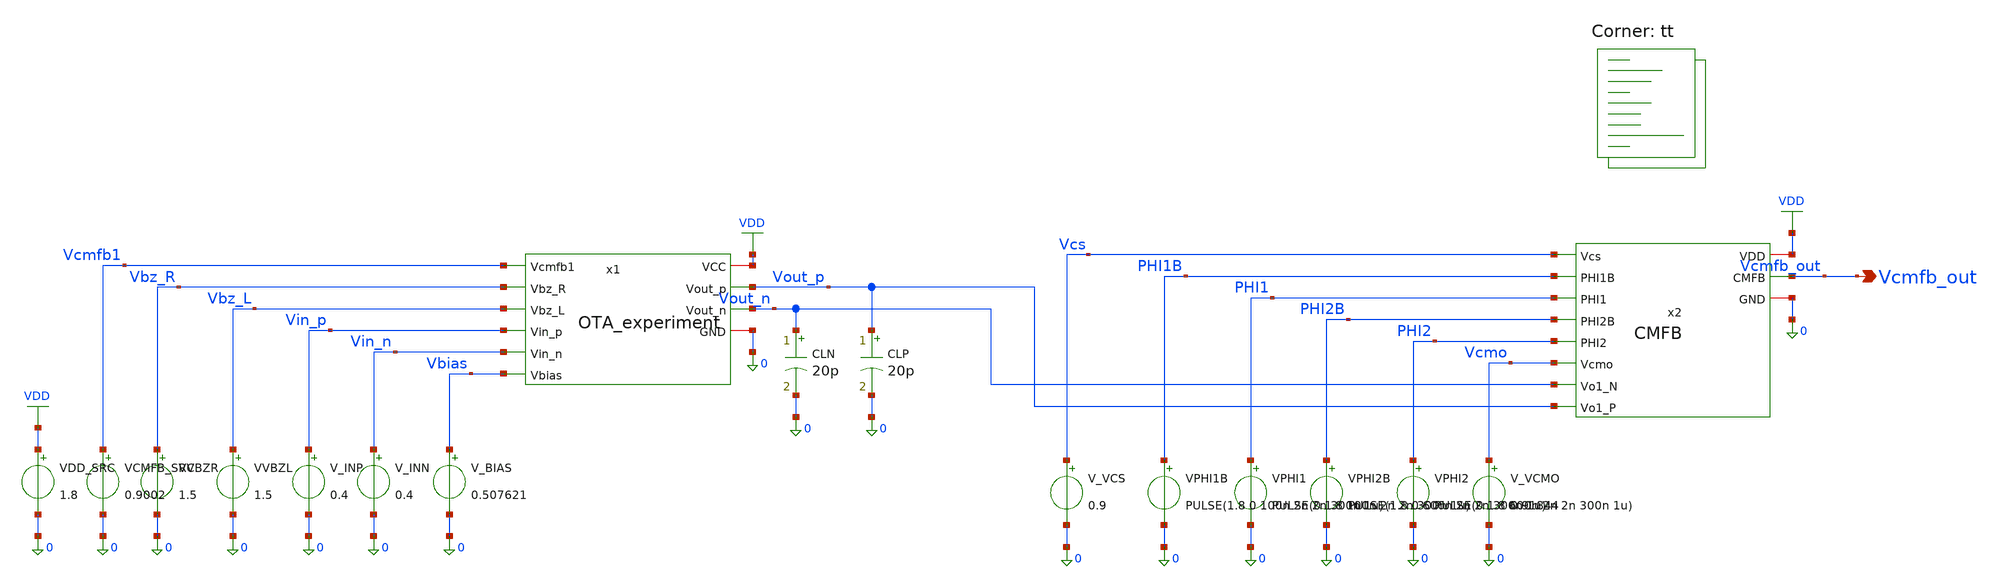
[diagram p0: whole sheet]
** sch_path: blocks/02_CMFB/sim/tb_OTA_CMFB_sign.sch
**.subckt tb_OTA_CMFB_sign Vcmfb_out
*.opin Vcmfb_out
VDD_SRC VDD 0 1.8
VCMFB_SRC Vcmfb1 0 0.9002
VVBZR Vbz_R 0 1.5
VVBZL Vbz_L 0 1.5
V_INP Vin_p 0 0.4
V_INN Vin_n 0 0.4
V_BIAS Vbias 0 0.507621
x1 VDD Vcmfb1 Vbz_R Vbz_L Vin_p Vin_n Vout_p Vout_n Vbias 0 OTA_experiment
CLP Vout_p 0 20p m=1
CLN Vout_n 0 20p m=1
V_VCS Vcs 0 0.9
VPHI1B PHI1B 0 PULSE(1.8 0 100n 2n 2n 300n 1u)
VPHI1 PHI1 0 PULSE(0 1.8 100n 2n 2n 300n 1u)
VPHI2B PHI2B 0 PULSE(1.8 0 600n 2n 2n 300n 1u)
VPHI2 PHI2 0 PULSE(0 1.8 600n 2n 2n 300n 1u)
V_VCMO Vcmo 0 0.91844
x2 Vcmfb_out Vcs PHI1B PHI1 VDD PHI2B 0 PHI2 Vcmo Vout_n Vout_p CMFB
**** begin user architecture code
.lib $::SKYWATER_MODELS/sky130.lib.spice tt


.options rshunt=1e12

RLEAK_OUT Vcmfb_out 0 1e12

.control
save all

* ==========================================================
* STEP 1: TRUE DC OPERATING POINT
* ==========================================================

op

let VOCM_OP = (v(vout_p)+v(vout_n))/2
let VOD_OP  = v(vout_p)-v(vout_n)

print v(vcmfb1)
print v(vout_p)
print v(vout_n)
print VOCM_OP
print VOD_OP


* ==========================================================
* STEP 2: TRANSIENT
*
* IMPORTANT:
* THERE IS NO UIC HERE.
* ==========================================================

tran 1n 10u

let VOCM = (v(vout_p)+v(vout_n))/2
let VOD  = v(vout_p)-v(vout_n)


* ==========================================================
* OTA STEADY-STATE CHARACTERIZATION
* ==========================================================

meas tran VOUTP_AVG AVG v(vout_p) FROM=8u TO=10u
meas tran VOUTN_AVG AVG v(vout_n) FROM=8u TO=10u

meas tran VOCM_AVG AVG VOCM FROM=8u TO=10u
meas tran VOCM_MIN MIN VOCM FROM=8u TO=10u
meas tran VOCM_MAX MAX VOCM FROM=8u TO=10u

meas tran VOD_AVG AVG VOD FROM=8u TO=10u


* ==========================================================
* EXTERNAL OTA CMFB CONTROL
* ==========================================================

meas tran VCMFB_IN_AVG AVG v(vcmfb1) FROM=8u TO=10u


* ==========================================================
* SC-CMFB OUTPUT CHARACTERIZATION
* ==========================================================

meas tran VCMFB_OUT_AVG AVG v(vcmfb_out) FROM=8u TO=10u
meas tran VCMFB_OUT_MIN MIN v(vcmfb_out) FROM=8u TO=10u
meas tran VCMFB_OUT_MAX MAX v(vcmfb_out) FROM=8u TO=10u

let VCMFB_OUT_RIPPLE = VCMFB_OUT_MAX-VCMFB_OUT_MIN

let VCMFB_OUT_ERROR = VCMFB_OUT_AVG-0.9


* ==========================================================
* CLOCK VALIDATION
* ==========================================================

meas tran PHI1_MAX MAX v(phi1)
meas tran PHI1_MIN MIN v(phi1)

meas tran PHI1B_MAX MAX v(phi1b)
meas tran PHI1B_MIN MIN v(phi1b)

meas tran PHI2_MAX MAX v(phi2)
meas tran PHI2_MIN MIN v(phi2)

meas tran PHI2B_MAX MAX v(phi2b)
meas tran PHI2B_MIN MIN v(phi2b)


* ==========================================================
* RESULTS
* ==========================================================

print VOUTP_AVG
print VOUTN_AVG

print VOCM_AVG
print VOCM_MIN
print VOCM_MAX
print VOD_AVG

print VCMFB_IN_AVG

print VCMFB_OUT_AVG
print VCMFB_OUT_MIN
print VCMFB_OUT_MAX
print VCMFB_OUT_RIPPLE
print VCMFB_OUT_ERROR

print PHI1_MAX
print PHI1_MIN

print PHI1B_MAX
print PHI1B_MIN

print PHI2_MAX
print PHI2_MIN

print PHI2B_MAX
print PHI2B_MIN


* ==========================================================
* PLOTS
* ==========================================================

plot v(phi1) v(phi2)
plot v(phi1b) v(phi2b)

plot v(vout_p) v(vout_n)

plot VOCM

plot v(vcmfb1) v(vcmfb_out)

.endc


**** end user architecture code
**.ends
.GLOBAL VDD
.end
